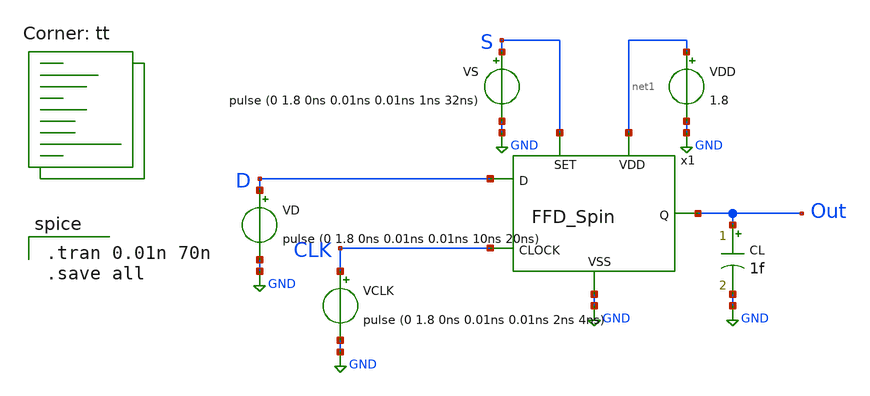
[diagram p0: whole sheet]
** sch_path: FFD_Spin_tb.sch
**.subckt FFD_Spin_tb
x1 net1 GND S CLK Out D FFD_Spin
CL Out GND 1f m=1
VD D GND pulse (0 1.8 0ns 0.01ns 0.01ns 10ns 20ns)
VCLK CLK GND pulse (0 1.8 0ns 0.01ns 0.01ns 2ns 4ns)
VS S GND pulse (0 1.8 0ns 0.01ns 0.01ns 1ns 32ns)
VDD net1 GND 1.8
**** begin user architecture code
.lib $::SKYWATER_MODELS/sky130.lib.spice tt

.tran 0.01n 70n
.save all

**** end user architecture code
**.ends
.GLOBAL GND
.end
